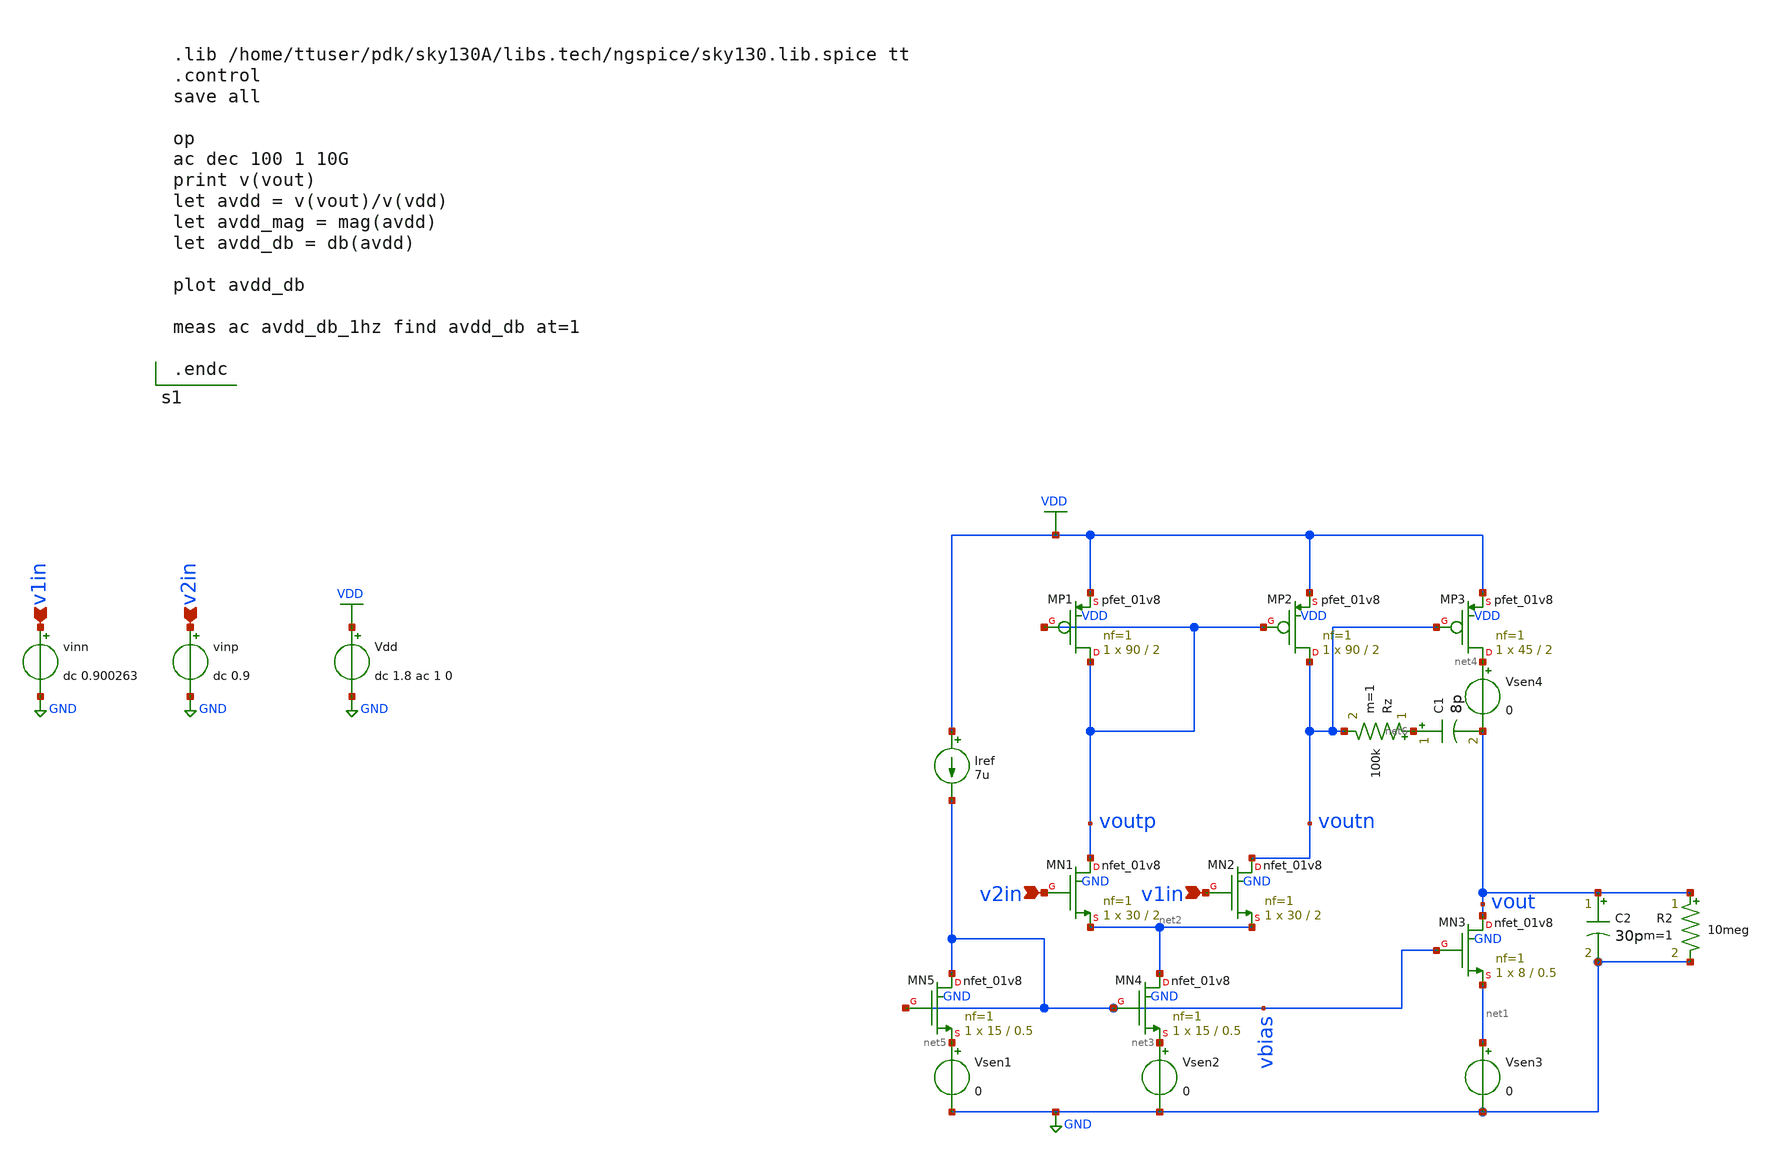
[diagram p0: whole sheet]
** sch_path: testbenches/prelayout/diffpairPSSRR.sch
**.subckt diffpairPSSRR v1in v1in v2in v2in
*.ipin v1in
*.ipin v1in
*.ipin v2in
*.ipin v2in
Vdd VDD GND dc 1.8 ac 1 0
vinp v2in GND dc 0.9
vinn v1in GND dc 0.900263
XMN1 voutp v2in net2 GND sky130_fd_pr__nfet_01v8 L=2 W=30 nf=1 ad='int((nf+1)/2) * W/nf * 0.29' as='int((nf+2)/2) * W/nf * 0.29'
+ pd='2*int((nf+1)/2) * (W/nf + 0.29)' ps='2*int((nf+2)/2) * (W/nf + 0.29)' nrd='0.29 / W' nrs='0.29 / W'
+ sa=0 sb=0 sd=0 mult=1 m=1
XMN2 voutn v1in net2 GND sky130_fd_pr__nfet_01v8 L=2 W=30 nf=1 ad='int((nf+1)/2) * W/nf * 0.29' as='int((nf+2)/2) * W/nf * 0.29'
+ pd='2*int((nf+1)/2) * (W/nf + 0.29)' ps='2*int((nf+2)/2) * (W/nf + 0.29)' nrd='0.29 / W' nrs='0.29 / W'
+ sa=0 sb=0 sd=0 mult=1 m=1
XMP1 voutp voutp VDD VDD sky130_fd_pr__pfet_01v8 L=2 W=90 nf=1 ad='int((nf+1)/2) * W/nf * 0.29' as='int((nf+2)/2) * W/nf * 0.29'
+ pd='2*int((nf+1)/2) * (W/nf + 0.29)' ps='2*int((nf+2)/2) * (W/nf + 0.29)' nrd='0.29 / W' nrs='0.29 / W'
+ sa=0 sb=0 sd=0 mult=1 m=1
XMP2 voutn voutp VDD VDD sky130_fd_pr__pfet_01v8 L=2 W=90 nf=1 ad='int((nf+1)/2) * W/nf * 0.29' as='int((nf+2)/2) * W/nf * 0.29'
+ pd='2*int((nf+1)/2) * (W/nf + 0.29)' ps='2*int((nf+2)/2) * (W/nf + 0.29)' nrd='0.29 / W' nrs='0.29 / W'
+ sa=0 sb=0 sd=0 mult=1 m=1
Iref VDD vbias 7u
Vsen2 net3 GND 0
XMP3 net4 voutn VDD VDD sky130_fd_pr__pfet_01v8 L=2 W=45 nf=1 ad='int((nf+1)/2) * W/nf * 0.29' as='int((nf+2)/2) * W/nf * 0.29'
+ pd='2*int((nf+1)/2) * (W/nf + 0.29)' ps='2*int((nf+2)/2) * (W/nf + 0.29)' nrd='0.29 / W' nrs='0.29 / W'
+ sa=0 sb=0 sd=0 mult=1 m=1
XMN3 vout vbias net1 GND sky130_fd_pr__nfet_01v8 L=0.5 W=8 nf=1 ad='int((nf+1)/2) * W/nf * 0.29' as='int((nf+2)/2) * W/nf * 0.29'
+ pd='2*int((nf+1)/2) * (W/nf + 0.29)' ps='2*int((nf+2)/2) * (W/nf + 0.29)' nrd='0.29 / W' nrs='0.29 / W'
+ sa=0 sb=0 sd=0 mult=1 m=1
Vsen3 net1 GND 0
Vsen1 net5 GND 0
C1 net6 vout 8p m=1
XMN4 net2 vbias net3 GND sky130_fd_pr__nfet_01v8 L=0.5 W=15 nf=1 ad='int((nf+1)/2) * W/nf * 0.29' as='int((nf+2)/2) * W/nf * 0.29'
+ pd='2*int((nf+1)/2) * (W/nf + 0.29)' ps='2*int((nf+2)/2) * (W/nf + 0.29)' nrd='0.29 / W' nrs='0.29 / W'
+ sa=0 sb=0 sd=0 mult=1 m=1
XMN5 vbias vbias net5 GND sky130_fd_pr__nfet_01v8 L=0.5 W=15 nf=1 ad='int((nf+1)/2) * W/nf * 0.29' as='int((nf+2)/2) * W/nf * 0.29'
+ pd='2*int((nf+1)/2) * (W/nf + 0.29)' ps='2*int((nf+2)/2) * (W/nf + 0.29)' nrd='0.29 / W' nrs='0.29 / W'
+ sa=0 sb=0 sd=0 mult=1 m=1
C2 vout GND 30p m=1
Rz net6 voutn 100k m=1
Vsen4 net4 vout 0
R2 vout GND 10meg m=1
**** begin user architecture code


.lib /home/ttuser/pdk/sky130A/libs.tech/ngspice/sky130.lib.spice tt
.control
save all

op
ac dec 100 1 10G
print v(vout)
let avdd = v(vout)/v(vdd)
let avdd_mag = mag(avdd)
let avdd_db = db(avdd)

plot avdd_db

meas ac avdd_db_1hz find avdd_db at=1

.endc


**** end user architecture code
**.ends
.GLOBAL VDD
.GLOBAL GND
.end
